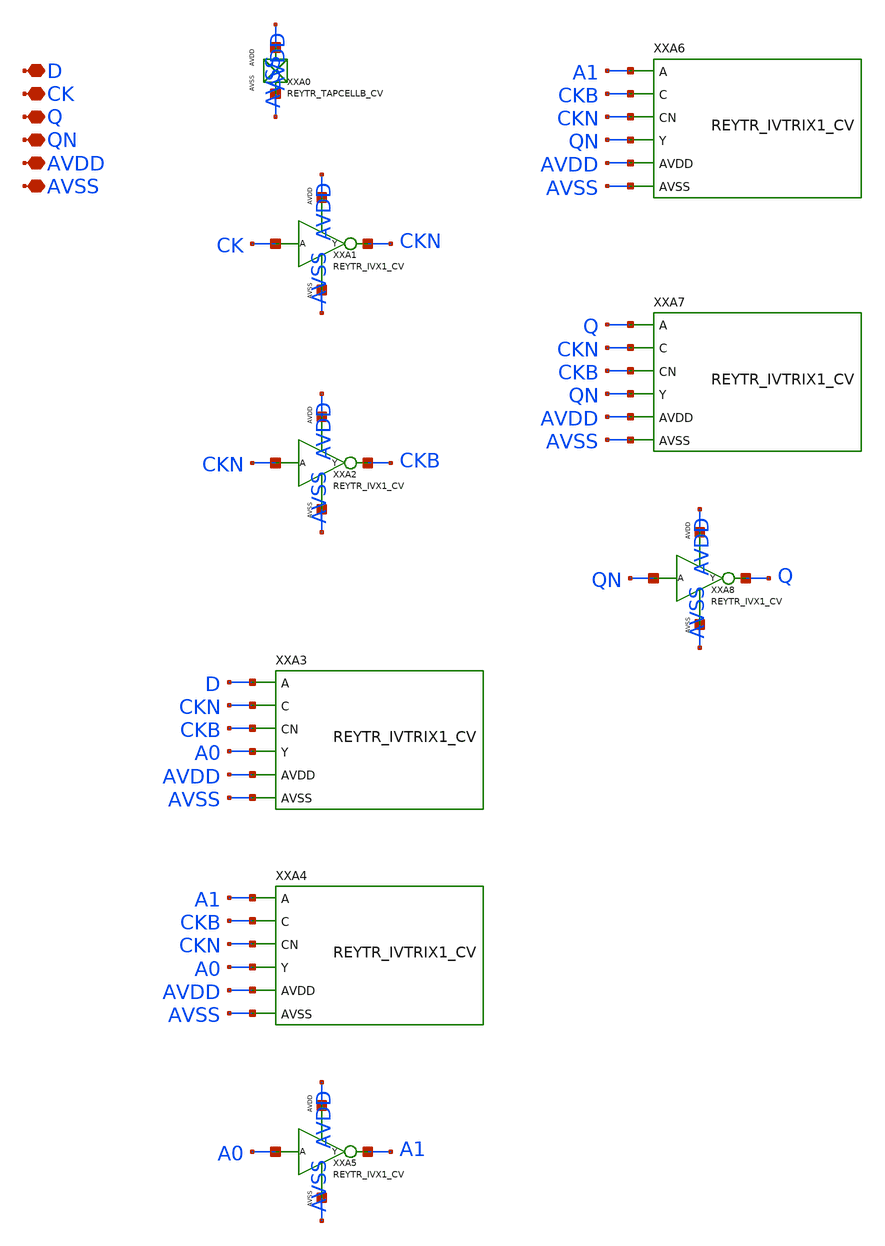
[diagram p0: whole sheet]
** sch_path: design/REY_TR_SKY130A/REYTR_DFQNX1_CV.sch
**.subckt REYTR_DFQNX1_CV D CK Q QN AVDD AVSS
*.iopin D
*.iopin CK
*.iopin Q
*.iopin QN
*.iopin AVDD
*.iopin AVSS
XXA0 AVDD AVSS REYTR_TAPCELLB_CV xoffset=0 yoffset=0 angle=0
XXA1 CK CKN AVDD AVSS REYTR_IVX1_CV
XXA2 CKN CKB AVDD AVSS REYTR_IVX1_CV
XXA3 D CKN CKB A0 AVDD AVSS REYTR_IVTRIX1_CV xoffset=0 yoffset=0 angle=0
XXA4 A1 CKB CKN A0 AVDD AVSS REYTR_IVTRIX1_CV xoffset=0 yoffset=0 angle=0
XXA5 A0 A1 AVDD AVSS REYTR_IVX1_CV
XXA6 A1 CKB CKN QN AVDD AVSS REYTR_IVTRIX1_CV xoffset=0 yoffset=0 angle=0
XXA7 Q CKN CKB QN AVDD AVSS REYTR_IVTRIX1_CV xoffset=0 yoffset=0 angle=0
XXA8 QN Q AVDD AVSS REYTR_IVX1_CV
**.ends
.end
